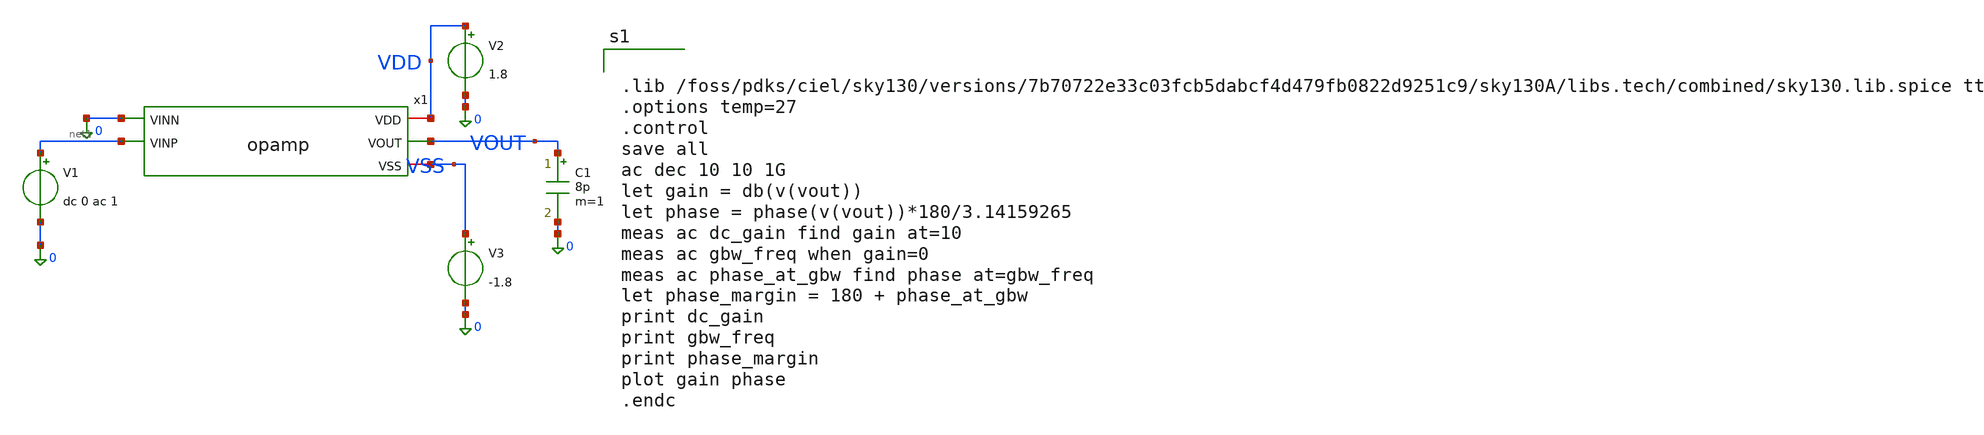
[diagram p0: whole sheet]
** sch_path: schematic/opamp_tb.sch
**.subckt opamp_tb
x1 VDD 0 net1 VOUT VSS opamp
V1 net1 0 dc 0 ac 1
V2 VDD 0 1.8
V3 VSS 0 -1.8
C1 VOUT 0 8p m=1
**** begin user architecture code


.lib /foss/pdks/ciel/sky130/versions/7b70722e33c03fcb5dabcf4d479fb0822d9251c9/sky130A/libs.tech/combined/sky130.lib.spice tt
.options temp=27
.control
save all
ac dec 10 10 1G
let gain = db(v(vout))
let phase = phase(v(vout))*180/3.14159265
meas ac dc_gain find gain at=10
meas ac gbw_freq when gain=0
meas ac phase_at_gbw find phase at=gbw_freq
let phase_margin = 180 + phase_at_gbw
print dc_gain
print gbw_freq
print phase_margin
plot gain phase
.endc


**** end user architecture code
**.ends

* expanding   symbol:  opamp.sym # of pins=5
** sym_path: schematic/opamp.sym
** sch_path: schematic/opamp.sch
.subckt opamp VDD VINN VINP VOUT VSS
*.ipin VINN
*.ipin VINP
*.iopin VSS
*.iopin VDD
*.opin VOUT
XM0 net2 net2 VSS VSS sky130_fd_pr__nfet_01v8 L=0.18 W=4 nf=2 ad='int((2 + 1)/2) * 4 / 2 * 0.29' as='int((2 + 2)/2) * 4 / 2 * 0.29'
+ pd='2*int((2 + 1)/2) * (4 / 2 + 0.29)' ps='2*int((2 + 2)/2) * (4 / 2 + 0.29)' nrd='0.29 / 4 ' nrs='0.29 / 4 '
+ sa=0 sb=0 sd=0 mult=1 m=1
XR1 net2 VDD VSS sky130_fd_pr__res_high_po_0p35 L=0.826 mult=1 m=1
XM1 net3 VINP net4 VSS sky130_fd_pr__nfet_01v8 L=0.18 W=150 nf=30 ad='int((30 + 1)/2) * 150 / 30 * 0.29'
+ as='int((30 + 2)/2) * 150 / 30 * 0.29' pd='2*int((30 + 1)/2) * (150 / 30 + 0.29)' ps='2*int((30 + 2)/2) * (150 / 30 + 0.29)'
+ nrd='0.29 / 150 ' nrs='0.29 / 150 ' sa=0 sb=0 sd=0 mult=1 m=1
XM2 net1 VINN net4 VSS sky130_fd_pr__nfet_01v8 L=0.18 W=150 nf=30 ad='int((30 + 1)/2) * 150 / 30 * 0.29'
+ as='int((30 + 2)/2) * 150 / 30 * 0.29' pd='2*int((30 + 1)/2) * (150 / 30 + 0.29)' ps='2*int((30 + 2)/2) * (150 / 30 + 0.29)'
+ nrd='0.29 / 150 ' nrs='0.29 / 150 ' sa=0 sb=0 sd=0 mult=1 m=1
XM3 net3 net3 VDD VDD sky130_fd_pr__pfet_01v8 L=0.18 W=4 nf=2 ad='int((2 + 1)/2) * 4 / 2 * 0.29' as='int((2 + 2)/2) * 4 / 2 * 0.29'
+ pd='2*int((2 + 1)/2) * (4 / 2 + 0.29)' ps='2*int((2 + 2)/2) * (4 / 2 + 0.29)' nrd='0.29 / 4 ' nrs='0.29 / 4 '
+ sa=0 sb=0 sd=0 mult=1 m=1
XM4 net1 net3 VDD VDD sky130_fd_pr__pfet_01v8 L=0.18 W=4 nf=2 ad='int((2 + 1)/2) * 4 / 2 * 0.29' as='int((2 + 2)/2) * 4 / 2 * 0.29'
+ pd='2*int((2 + 1)/2) * (4 / 2 + 0.29)' ps='2*int((2 + 2)/2) * (4 / 2 + 0.29)' nrd='0.29 / 4 ' nrs='0.29 / 4 '
+ sa=0 sb=0 sd=0 mult=1 m=1
XM5 net4 net2 VSS VSS sky130_fd_pr__nfet_01v8 L=0.18 W=4 nf=2 ad='int((2 + 1)/2) * 4 / 2 * 0.29' as='int((2 + 2)/2) * 4 / 2 * 0.29'
+ pd='2*int((2 + 1)/2) * (4 / 2 + 0.29)' ps='2*int((2 + 2)/2) * (4 / 2 + 0.29)' nrd='0.29 / 4 ' nrs='0.29 / 4 '
+ sa=0 sb=0 sd=0 mult=1 m=1
XM6 VOUT net1 VDD VDD sky130_fd_pr__pfet_01v8 L=0.18 W=4 nf=2 ad='int((2 + 1)/2) * 4 / 2 * 0.29' as='int((2 + 2)/2) * 4 / 2 * 0.29'
+ pd='2*int((2 + 1)/2) * (4 / 2 + 0.29)' ps='2*int((2 + 2)/2) * (4 / 2 + 0.29)' nrd='0.29 / 4 ' nrs='0.29 / 4 '
+ sa=0 sb=0 sd=0 mult=1 m=1
XM7 VOUT net2 VSS VSS sky130_fd_pr__nfet_01v8 L=0.18 W=4 nf=2 ad='int((2 + 1)/2) * 4 / 2 * 0.29' as='int((2 + 2)/2) * 4 / 2 * 0.29'
+ pd='2*int((2 + 1)/2) * (4 / 2 + 0.29)' ps='2*int((2 + 2)/2) * (4 / 2 + 0.29)' nrd='0.29 / 4 ' nrs='0.29 / 4 '
+ sa=0 sb=0 sd=0 mult=1 m=1
XC1 net1 VOUT sky130_fd_pr__cap_mim_m3_1 W=2.8 L=2.8 MF=1 m=1
.ends

.end
